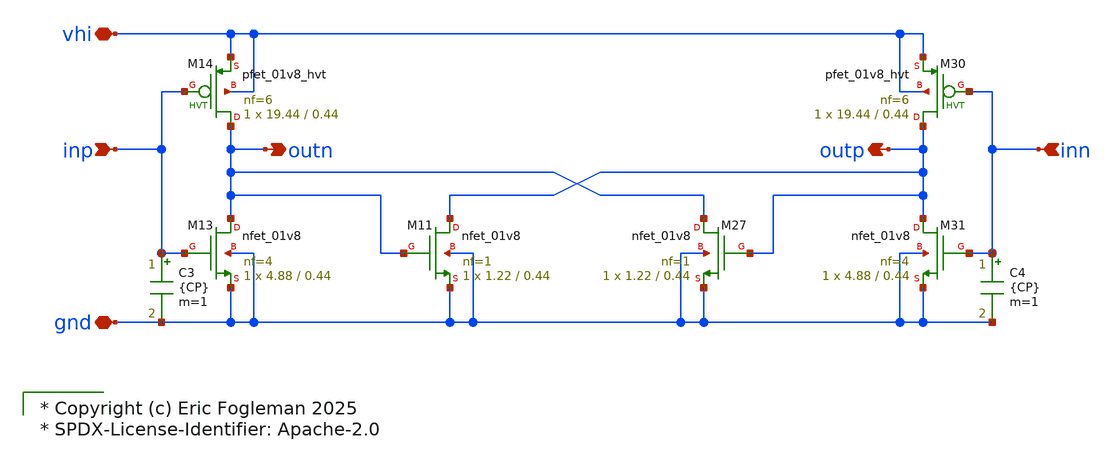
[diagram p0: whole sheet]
** sch_path: xschem/ejf_pll96_vco_dlycell.sch

* Copyright (c) Eric Fogleman 2025
* SPDX-License-Identifier: Apache-2.0

**.subckt ejf_pll96_vco_dlycell inp outn inn outp vhi gnd
*.ipin inp
*.opin outn
*.ipin inn
*.opin outp
*.iopin vhi
*.iopin gnd
XM11 outp outn gnd gnd sky130_fd_pr__nfet_01v8 L=0.44 W=1.22 nf=1 ad='int((nf+1)/2) * W/nf * 0.29' as='int((nf+2)/2) * W/nf * 0.29'
+ pd='2*int((nf+1)/2) * (W/nf + 0.29)' ps='2*int((nf+2)/2) * (W/nf + 0.29)' nrd='0.29 / W' nrs='0.29 / W'
+ sa=0 sb=0 sd=0 mult=1 m=1
XM13 outn inp gnd gnd sky130_fd_pr__nfet_01v8 L=0.44 W=4.88 nf=4 ad='int((nf+1)/2) * W/nf * 0.29' as='int((nf+2)/2) * W/nf * 0.29'
+ pd='2*int((nf+1)/2) * (W/nf + 0.29)' ps='2*int((nf+2)/2) * (W/nf + 0.29)' nrd='0.29 / W' nrs='0.29 / W'
+ sa=0 sb=0 sd=0 mult=1 m=1
XM14 outn inp vhi vhi sky130_fd_pr__pfet_01v8_hvt L=0.44 W=19.44 nf=6 ad='int((nf+1)/2) * W/nf * 0.29'
+ as='int((nf+2)/2) * W/nf * 0.29' pd='2*int((nf+1)/2) * (W/nf + 0.29)' ps='2*int((nf+2)/2) * (W/nf + 0.29)'
+ nrd='0.29 / W' nrs='0.29 / W' sa=0 sb=0 sd=0 mult=1 m=1
XM27 outn outp gnd gnd sky130_fd_pr__nfet_01v8 L=0.44 W=1.22 nf=1 ad='int((nf+1)/2) * W/nf * 0.29' as='int((nf+2)/2) * W/nf * 0.29'
+ pd='2*int((nf+1)/2) * (W/nf + 0.29)' ps='2*int((nf+2)/2) * (W/nf + 0.29)' nrd='0.29 / W' nrs='0.29 / W'
+ sa=0 sb=0 sd=0 mult=1 m=1
XM31 outp inn gnd gnd sky130_fd_pr__nfet_01v8 L=0.44 W=4.88 nf=4 ad='int((nf+1)/2) * W/nf * 0.29' as='int((nf+2)/2) * W/nf * 0.29'
+ pd='2*int((nf+1)/2) * (W/nf + 0.29)' ps='2*int((nf+2)/2) * (W/nf + 0.29)' nrd='0.29 / W' nrs='0.29 / W'
+ sa=0 sb=0 sd=0 mult=1 m=1
XM30 outp inn vhi vhi sky130_fd_pr__pfet_01v8_hvt L=0.44 W=19.44 nf=6 ad='int((nf+1)/2) * W/nf * 0.29'
+ as='int((nf+2)/2) * W/nf * 0.29' pd='2*int((nf+1)/2) * (W/nf + 0.29)' ps='2*int((nf+2)/2) * (W/nf + 0.29)'
+ nrd='0.29 / W' nrs='0.29 / W' sa=0 sb=0 sd=0 mult=1 m=1
C3 inp gnd {CP} m=1
C4 inn gnd {CP} m=1
**.ends
.end
